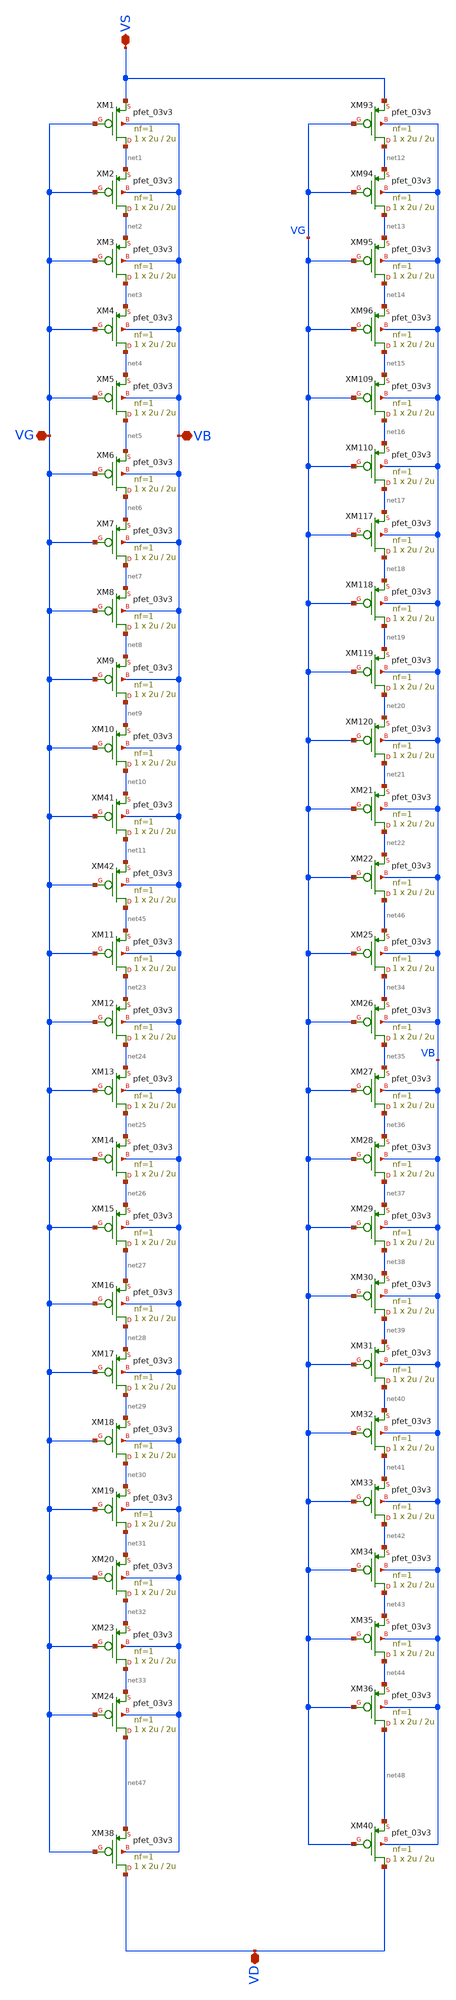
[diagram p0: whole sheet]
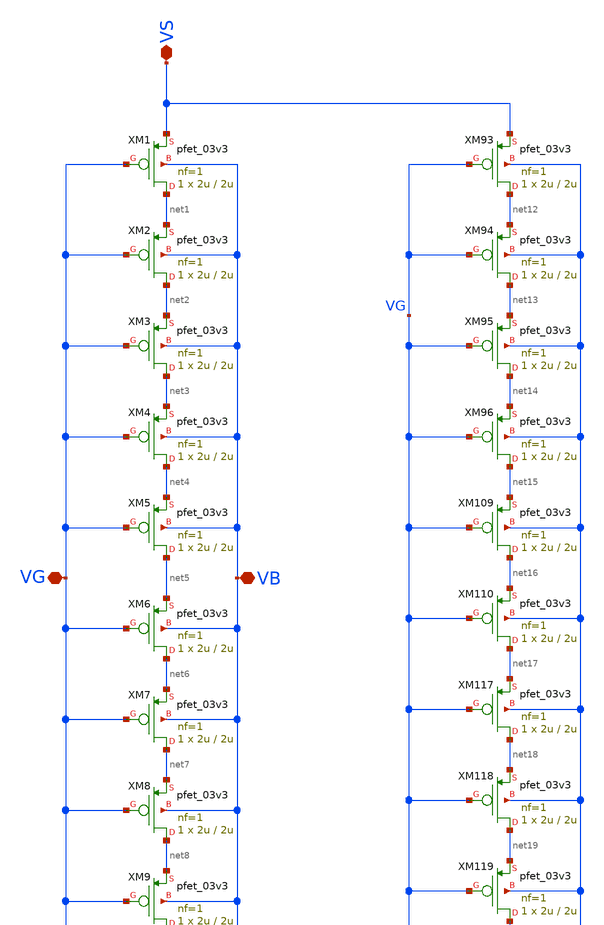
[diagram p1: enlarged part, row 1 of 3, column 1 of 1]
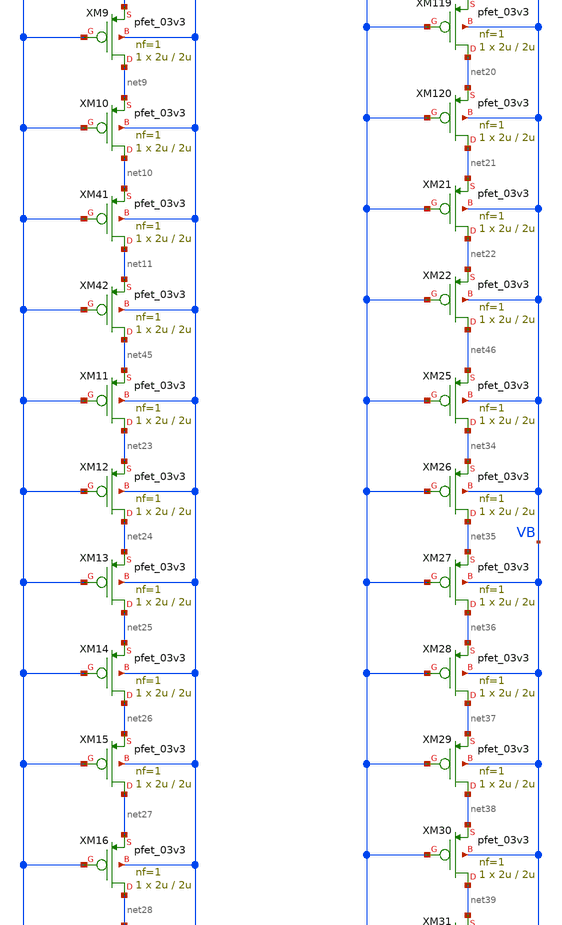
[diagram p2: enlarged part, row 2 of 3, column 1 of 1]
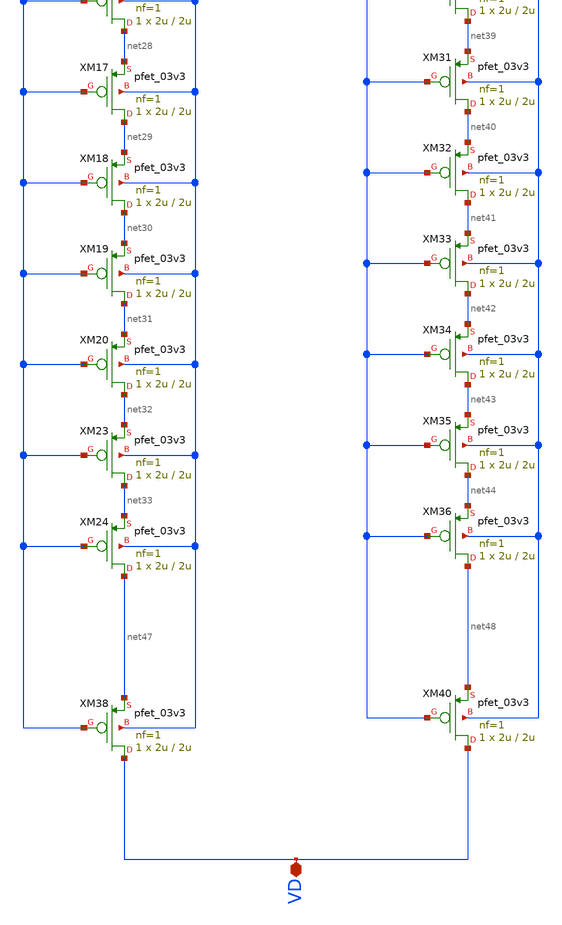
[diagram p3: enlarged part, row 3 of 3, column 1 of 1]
** sch_path: Voltage_Reference/symbols_vr/PMOS_association_1_12.sch
**.subckt PMOS_association_1_12 VD VB VG VS
*.iopin VD
*.iopin VB
*.iopin VG
*.iopin VS
XM1 net1 VG VS VB pfet_03v3 L=2u W=2u nf=1 ad='int((nf+1)/2) * W/nf * 0.18u' as='int((nf+2)/2) * W/nf * 0.18u'
+ pd='2*int((nf+1)/2) * (W/nf + 0.18u)' ps='2*int((nf+2)/2) * (W/nf + 0.18u)' nrd='0.18u / W' nrs='0.18u / W'
+ sa=0 sb=0 sd=0 m=1
XM2 net2 VG net1 VB pfet_03v3 L=2u W=2u nf=1 ad='int((nf+1)/2) * W/nf * 0.18u' as='int((nf+2)/2) * W/nf * 0.18u'
+ pd='2*int((nf+1)/2) * (W/nf + 0.18u)' ps='2*int((nf+2)/2) * (W/nf + 0.18u)' nrd='0.18u / W' nrs='0.18u / W'
+ sa=0 sb=0 sd=0 m=1
XM3 net3 VG net2 VB pfet_03v3 L=2u W=2u nf=1 ad='int((nf+1)/2) * W/nf * 0.18u' as='int((nf+2)/2) * W/nf * 0.18u'
+ pd='2*int((nf+1)/2) * (W/nf + 0.18u)' ps='2*int((nf+2)/2) * (W/nf + 0.18u)' nrd='0.18u / W' nrs='0.18u / W'
+ sa=0 sb=0 sd=0 m=1
XM4 net4 VG net3 VB pfet_03v3 L=2u W=2u nf=1 ad='int((nf+1)/2) * W/nf * 0.18u' as='int((nf+2)/2) * W/nf * 0.18u'
+ pd='2*int((nf+1)/2) * (W/nf + 0.18u)' ps='2*int((nf+2)/2) * (W/nf + 0.18u)' nrd='0.18u / W' nrs='0.18u / W'
+ sa=0 sb=0 sd=0 m=1
XM5 net5 VG net4 VB pfet_03v3 L=2u W=2u nf=1 ad='int((nf+1)/2) * W/nf * 0.18u' as='int((nf+2)/2) * W/nf * 0.18u'
+ pd='2*int((nf+1)/2) * (W/nf + 0.18u)' ps='2*int((nf+2)/2) * (W/nf + 0.18u)' nrd='0.18u / W' nrs='0.18u / W'
+ sa=0 sb=0 sd=0 m=1
XM6 net6 VG net5 VB pfet_03v3 L=2u W=2u nf=1 ad='int((nf+1)/2) * W/nf * 0.18u' as='int((nf+2)/2) * W/nf * 0.18u'
+ pd='2*int((nf+1)/2) * (W/nf + 0.18u)' ps='2*int((nf+2)/2) * (W/nf + 0.18u)' nrd='0.18u / W' nrs='0.18u / W'
+ sa=0 sb=0 sd=0 m=1
XM7 net7 VG net6 VB pfet_03v3 L=2u W=2u nf=1 ad='int((nf+1)/2) * W/nf * 0.18u' as='int((nf+2)/2) * W/nf * 0.18u'
+ pd='2*int((nf+1)/2) * (W/nf + 0.18u)' ps='2*int((nf+2)/2) * (W/nf + 0.18u)' nrd='0.18u / W' nrs='0.18u / W'
+ sa=0 sb=0 sd=0 m=1
XM8 net8 VG net7 VB pfet_03v3 L=2u W=2u nf=1 ad='int((nf+1)/2) * W/nf * 0.18u' as='int((nf+2)/2) * W/nf * 0.18u'
+ pd='2*int((nf+1)/2) * (W/nf + 0.18u)' ps='2*int((nf+2)/2) * (W/nf + 0.18u)' nrd='0.18u / W' nrs='0.18u / W'
+ sa=0 sb=0 sd=0 m=1
XM9 net9 VG net8 VB pfet_03v3 L=2u W=2u nf=1 ad='int((nf+1)/2) * W/nf * 0.18u' as='int((nf+2)/2) * W/nf * 0.18u'
+ pd='2*int((nf+1)/2) * (W/nf + 0.18u)' ps='2*int((nf+2)/2) * (W/nf + 0.18u)' nrd='0.18u / W' nrs='0.18u / W'
+ sa=0 sb=0 sd=0 m=1
XM10 net10 VG net9 VB pfet_03v3 L=2u W=2u nf=1 ad='int((nf+1)/2) * W/nf * 0.18u' as='int((nf+2)/2) * W/nf * 0.18u'
+ pd='2*int((nf+1)/2) * (W/nf + 0.18u)' ps='2*int((nf+2)/2) * (W/nf + 0.18u)' nrd='0.18u / W' nrs='0.18u / W'
+ sa=0 sb=0 sd=0 m=1
XM41 net11 VG net10 VB pfet_03v3 L=2u W=2u nf=1 ad='int((nf+1)/2) * W/nf * 0.18u' as='int((nf+2)/2) * W/nf * 0.18u'
+ pd='2*int((nf+1)/2) * (W/nf + 0.18u)' ps='2*int((nf+2)/2) * (W/nf + 0.18u)' nrd='0.18u / W' nrs='0.18u / W'
+ sa=0 sb=0 sd=0 m=1
XM42 net45 VG net11 VB pfet_03v3 L=2u W=2u nf=1 ad='int((nf+1)/2) * W/nf * 0.18u' as='int((nf+2)/2) * W/nf * 0.18u'
+ pd='2*int((nf+1)/2) * (W/nf + 0.18u)' ps='2*int((nf+2)/2) * (W/nf + 0.18u)' nrd='0.18u / W' nrs='0.18u / W'
+ sa=0 sb=0 sd=0 m=1
XM93 net12 VG VS VB pfet_03v3 L=2u W=2u nf=1 ad='int((nf+1)/2) * W/nf * 0.18u' as='int((nf+2)/2) * W/nf * 0.18u'
+ pd='2*int((nf+1)/2) * (W/nf + 0.18u)' ps='2*int((nf+2)/2) * (W/nf + 0.18u)' nrd='0.18u / W' nrs='0.18u / W'
+ sa=0 sb=0 sd=0 m=1
XM94 net13 VG net12 VB pfet_03v3 L=2u W=2u nf=1 ad='int((nf+1)/2) * W/nf * 0.18u' as='int((nf+2)/2) * W/nf * 0.18u'
+ pd='2*int((nf+1)/2) * (W/nf + 0.18u)' ps='2*int((nf+2)/2) * (W/nf + 0.18u)' nrd='0.18u / W' nrs='0.18u / W'
+ sa=0 sb=0 sd=0 m=1
XM95 net14 VG net13 VB pfet_03v3 L=2u W=2u nf=1 ad='int((nf+1)/2) * W/nf * 0.18u' as='int((nf+2)/2) * W/nf * 0.18u'
+ pd='2*int((nf+1)/2) * (W/nf + 0.18u)' ps='2*int((nf+2)/2) * (W/nf + 0.18u)' nrd='0.18u / W' nrs='0.18u / W'
+ sa=0 sb=0 sd=0 m=1
XM96 net15 VG net14 VB pfet_03v3 L=2u W=2u nf=1 ad='int((nf+1)/2) * W/nf * 0.18u' as='int((nf+2)/2) * W/nf * 0.18u'
+ pd='2*int((nf+1)/2) * (W/nf + 0.18u)' ps='2*int((nf+2)/2) * (W/nf + 0.18u)' nrd='0.18u / W' nrs='0.18u / W'
+ sa=0 sb=0 sd=0 m=1
XM109 net16 VG net15 VB pfet_03v3 L=2u W=2u nf=1 ad='int((nf+1)/2) * W/nf * 0.18u' as='int((nf+2)/2) * W/nf * 0.18u'
+ pd='2*int((nf+1)/2) * (W/nf + 0.18u)' ps='2*int((nf+2)/2) * (W/nf + 0.18u)' nrd='0.18u / W' nrs='0.18u / W'
+ sa=0 sb=0 sd=0 m=1
XM110 net17 VG net16 VB pfet_03v3 L=2u W=2u nf=1 ad='int((nf+1)/2) * W/nf * 0.18u' as='int((nf+2)/2) * W/nf * 0.18u'
+ pd='2*int((nf+1)/2) * (W/nf + 0.18u)' ps='2*int((nf+2)/2) * (W/nf + 0.18u)' nrd='0.18u / W' nrs='0.18u / W'
+ sa=0 sb=0 sd=0 m=1
XM117 net18 VG net17 VB pfet_03v3 L=2u W=2u nf=1 ad='int((nf+1)/2) * W/nf * 0.18u' as='int((nf+2)/2) * W/nf * 0.18u'
+ pd='2*int((nf+1)/2) * (W/nf + 0.18u)' ps='2*int((nf+2)/2) * (W/nf + 0.18u)' nrd='0.18u / W' nrs='0.18u / W'
+ sa=0 sb=0 sd=0 m=1
XM118 net19 VG net18 VB pfet_03v3 L=2u W=2u nf=1 ad='int((nf+1)/2) * W/nf * 0.18u' as='int((nf+2)/2) * W/nf * 0.18u'
+ pd='2*int((nf+1)/2) * (W/nf + 0.18u)' ps='2*int((nf+2)/2) * (W/nf + 0.18u)' nrd='0.18u / W' nrs='0.18u / W'
+ sa=0 sb=0 sd=0 m=1
XM119 net20 VG net19 VB pfet_03v3 L=2u W=2u nf=1 ad='int((nf+1)/2) * W/nf * 0.18u' as='int((nf+2)/2) * W/nf * 0.18u'
+ pd='2*int((nf+1)/2) * (W/nf + 0.18u)' ps='2*int((nf+2)/2) * (W/nf + 0.18u)' nrd='0.18u / W' nrs='0.18u / W'
+ sa=0 sb=0 sd=0 m=1
XM120 net21 VG net20 VB pfet_03v3 L=2u W=2u nf=1 ad='int((nf+1)/2) * W/nf * 0.18u' as='int((nf+2)/2) * W/nf * 0.18u'
+ pd='2*int((nf+1)/2) * (W/nf + 0.18u)' ps='2*int((nf+2)/2) * (W/nf + 0.18u)' nrd='0.18u / W' nrs='0.18u / W'
+ sa=0 sb=0 sd=0 m=1
XM21 net22 VG net21 VB pfet_03v3 L=2u W=2u nf=1 ad='int((nf+1)/2) * W/nf * 0.18u' as='int((nf+2)/2) * W/nf * 0.18u'
+ pd='2*int((nf+1)/2) * (W/nf + 0.18u)' ps='2*int((nf+2)/2) * (W/nf + 0.18u)' nrd='0.18u / W' nrs='0.18u / W'
+ sa=0 sb=0 sd=0 m=1
XM22 net46 VG net22 VB pfet_03v3 L=2u W=2u nf=1 ad='int((nf+1)/2) * W/nf * 0.18u' as='int((nf+2)/2) * W/nf * 0.18u'
+ pd='2*int((nf+1)/2) * (W/nf + 0.18u)' ps='2*int((nf+2)/2) * (W/nf + 0.18u)' nrd='0.18u / W' nrs='0.18u / W'
+ sa=0 sb=0 sd=0 m=1
XM11 net23 VG net45 VB pfet_03v3 L=2u W=2u nf=1 ad='int((nf+1)/2) * W/nf * 0.18u' as='int((nf+2)/2) * W/nf * 0.18u'
+ pd='2*int((nf+1)/2) * (W/nf + 0.18u)' ps='2*int((nf+2)/2) * (W/nf + 0.18u)' nrd='0.18u / W' nrs='0.18u / W'
+ sa=0 sb=0 sd=0 m=1
XM12 net24 VG net23 VB pfet_03v3 L=2u W=2u nf=1 ad='int((nf+1)/2) * W/nf * 0.18u' as='int((nf+2)/2) * W/nf * 0.18u'
+ pd='2*int((nf+1)/2) * (W/nf + 0.18u)' ps='2*int((nf+2)/2) * (W/nf + 0.18u)' nrd='0.18u / W' nrs='0.18u / W'
+ sa=0 sb=0 sd=0 m=1
XM13 net25 VG net24 VB pfet_03v3 L=2u W=2u nf=1 ad='int((nf+1)/2) * W/nf * 0.18u' as='int((nf+2)/2) * W/nf * 0.18u'
+ pd='2*int((nf+1)/2) * (W/nf + 0.18u)' ps='2*int((nf+2)/2) * (W/nf + 0.18u)' nrd='0.18u / W' nrs='0.18u / W'
+ sa=0 sb=0 sd=0 m=1
XM14 net26 VG net25 VB pfet_03v3 L=2u W=2u nf=1 ad='int((nf+1)/2) * W/nf * 0.18u' as='int((nf+2)/2) * W/nf * 0.18u'
+ pd='2*int((nf+1)/2) * (W/nf + 0.18u)' ps='2*int((nf+2)/2) * (W/nf + 0.18u)' nrd='0.18u / W' nrs='0.18u / W'
+ sa=0 sb=0 sd=0 m=1
XM15 net27 VG net26 VB pfet_03v3 L=2u W=2u nf=1 ad='int((nf+1)/2) * W/nf * 0.18u' as='int((nf+2)/2) * W/nf * 0.18u'
+ pd='2*int((nf+1)/2) * (W/nf + 0.18u)' ps='2*int((nf+2)/2) * (W/nf + 0.18u)' nrd='0.18u / W' nrs='0.18u / W'
+ sa=0 sb=0 sd=0 m=1
XM16 net28 VG net27 VB pfet_03v3 L=2u W=2u nf=1 ad='int((nf+1)/2) * W/nf * 0.18u' as='int((nf+2)/2) * W/nf * 0.18u'
+ pd='2*int((nf+1)/2) * (W/nf + 0.18u)' ps='2*int((nf+2)/2) * (W/nf + 0.18u)' nrd='0.18u / W' nrs='0.18u / W'
+ sa=0 sb=0 sd=0 m=1
XM17 net29 VG net28 VB pfet_03v3 L=2u W=2u nf=1 ad='int((nf+1)/2) * W/nf * 0.18u' as='int((nf+2)/2) * W/nf * 0.18u'
+ pd='2*int((nf+1)/2) * (W/nf + 0.18u)' ps='2*int((nf+2)/2) * (W/nf + 0.18u)' nrd='0.18u / W' nrs='0.18u / W'
+ sa=0 sb=0 sd=0 m=1
XM18 net30 VG net29 VB pfet_03v3 L=2u W=2u nf=1 ad='int((nf+1)/2) * W/nf * 0.18u' as='int((nf+2)/2) * W/nf * 0.18u'
+ pd='2*int((nf+1)/2) * (W/nf + 0.18u)' ps='2*int((nf+2)/2) * (W/nf + 0.18u)' nrd='0.18u / W' nrs='0.18u / W'
+ sa=0 sb=0 sd=0 m=1
XM19 net31 VG net30 VB pfet_03v3 L=2u W=2u nf=1 ad='int((nf+1)/2) * W/nf * 0.18u' as='int((nf+2)/2) * W/nf * 0.18u'
+ pd='2*int((nf+1)/2) * (W/nf + 0.18u)' ps='2*int((nf+2)/2) * (W/nf + 0.18u)' nrd='0.18u / W' nrs='0.18u / W'
+ sa=0 sb=0 sd=0 m=1
XM20 net32 VG net31 VB pfet_03v3 L=2u W=2u nf=1 ad='int((nf+1)/2) * W/nf * 0.18u' as='int((nf+2)/2) * W/nf * 0.18u'
+ pd='2*int((nf+1)/2) * (W/nf + 0.18u)' ps='2*int((nf+2)/2) * (W/nf + 0.18u)' nrd='0.18u / W' nrs='0.18u / W'
+ sa=0 sb=0 sd=0 m=1
XM23 net33 VG net32 VB pfet_03v3 L=2u W=2u nf=1 ad='int((nf+1)/2) * W/nf * 0.18u' as='int((nf+2)/2) * W/nf * 0.18u'
+ pd='2*int((nf+1)/2) * (W/nf + 0.18u)' ps='2*int((nf+2)/2) * (W/nf + 0.18u)' nrd='0.18u / W' nrs='0.18u / W'
+ sa=0 sb=0 sd=0 m=1
XM24 net47 VG net33 VB pfet_03v3 L=2u W=2u nf=1 ad='int((nf+1)/2) * W/nf * 0.18u' as='int((nf+2)/2) * W/nf * 0.18u'
+ pd='2*int((nf+1)/2) * (W/nf + 0.18u)' ps='2*int((nf+2)/2) * (W/nf + 0.18u)' nrd='0.18u / W' nrs='0.18u / W'
+ sa=0 sb=0 sd=0 m=1
XM25 net34 VG net46 VB pfet_03v3 L=2u W=2u nf=1 ad='int((nf+1)/2) * W/nf * 0.18u' as='int((nf+2)/2) * W/nf * 0.18u'
+ pd='2*int((nf+1)/2) * (W/nf + 0.18u)' ps='2*int((nf+2)/2) * (W/nf + 0.18u)' nrd='0.18u / W' nrs='0.18u / W'
+ sa=0 sb=0 sd=0 m=1
XM26 net35 VG net34 VB pfet_03v3 L=2u W=2u nf=1 ad='int((nf+1)/2) * W/nf * 0.18u' as='int((nf+2)/2) * W/nf * 0.18u'
+ pd='2*int((nf+1)/2) * (W/nf + 0.18u)' ps='2*int((nf+2)/2) * (W/nf + 0.18u)' nrd='0.18u / W' nrs='0.18u / W'
+ sa=0 sb=0 sd=0 m=1
XM27 net36 VG net35 VB pfet_03v3 L=2u W=2u nf=1 ad='int((nf+1)/2) * W/nf * 0.18u' as='int((nf+2)/2) * W/nf * 0.18u'
+ pd='2*int((nf+1)/2) * (W/nf + 0.18u)' ps='2*int((nf+2)/2) * (W/nf + 0.18u)' nrd='0.18u / W' nrs='0.18u / W'
+ sa=0 sb=0 sd=0 m=1
XM28 net37 VG net36 VB pfet_03v3 L=2u W=2u nf=1 ad='int((nf+1)/2) * W/nf * 0.18u' as='int((nf+2)/2) * W/nf * 0.18u'
+ pd='2*int((nf+1)/2) * (W/nf + 0.18u)' ps='2*int((nf+2)/2) * (W/nf + 0.18u)' nrd='0.18u / W' nrs='0.18u / W'
+ sa=0 sb=0 sd=0 m=1
XM29 net38 VG net37 VB pfet_03v3 L=2u W=2u nf=1 ad='int((nf+1)/2) * W/nf * 0.18u' as='int((nf+2)/2) * W/nf * 0.18u'
+ pd='2*int((nf+1)/2) * (W/nf + 0.18u)' ps='2*int((nf+2)/2) * (W/nf + 0.18u)' nrd='0.18u / W' nrs='0.18u / W'
+ sa=0 sb=0 sd=0 m=1
XM30 net39 VG net38 VB pfet_03v3 L=2u W=2u nf=1 ad='int((nf+1)/2) * W/nf * 0.18u' as='int((nf+2)/2) * W/nf * 0.18u'
+ pd='2*int((nf+1)/2) * (W/nf + 0.18u)' ps='2*int((nf+2)/2) * (W/nf + 0.18u)' nrd='0.18u / W' nrs='0.18u / W'
+ sa=0 sb=0 sd=0 m=1
XM31 net40 VG net39 VB pfet_03v3 L=2u W=2u nf=1 ad='int((nf+1)/2) * W/nf * 0.18u' as='int((nf+2)/2) * W/nf * 0.18u'
+ pd='2*int((nf+1)/2) * (W/nf + 0.18u)' ps='2*int((nf+2)/2) * (W/nf + 0.18u)' nrd='0.18u / W' nrs='0.18u / W'
+ sa=0 sb=0 sd=0 m=1
XM32 net41 VG net40 VB pfet_03v3 L=2u W=2u nf=1 ad='int((nf+1)/2) * W/nf * 0.18u' as='int((nf+2)/2) * W/nf * 0.18u'
+ pd='2*int((nf+1)/2) * (W/nf + 0.18u)' ps='2*int((nf+2)/2) * (W/nf + 0.18u)' nrd='0.18u / W' nrs='0.18u / W'
+ sa=0 sb=0 sd=0 m=1
XM33 net42 VG net41 VB pfet_03v3 L=2u W=2u nf=1 ad='int((nf+1)/2) * W/nf * 0.18u' as='int((nf+2)/2) * W/nf * 0.18u'
+ pd='2*int((nf+1)/2) * (W/nf + 0.18u)' ps='2*int((nf+2)/2) * (W/nf + 0.18u)' nrd='0.18u / W' nrs='0.18u / W'
+ sa=0 sb=0 sd=0 m=1
XM34 net43 VG net42 VB pfet_03v3 L=2u W=2u nf=1 ad='int((nf+1)/2) * W/nf * 0.18u' as='int((nf+2)/2) * W/nf * 0.18u'
+ pd='2*int((nf+1)/2) * (W/nf + 0.18u)' ps='2*int((nf+2)/2) * (W/nf + 0.18u)' nrd='0.18u / W' nrs='0.18u / W'
+ sa=0 sb=0 sd=0 m=1
XM35 net44 VG net43 VB pfet_03v3 L=2u W=2u nf=1 ad='int((nf+1)/2) * W/nf * 0.18u' as='int((nf+2)/2) * W/nf * 0.18u'
+ pd='2*int((nf+1)/2) * (W/nf + 0.18u)' ps='2*int((nf+2)/2) * (W/nf + 0.18u)' nrd='0.18u / W' nrs='0.18u / W'
+ sa=0 sb=0 sd=0 m=1
XM36 net48 VG net44 VB pfet_03v3 L=2u W=2u nf=1 ad='int((nf+1)/2) * W/nf * 0.18u' as='int((nf+2)/2) * W/nf * 0.18u'
+ pd='2*int((nf+1)/2) * (W/nf + 0.18u)' ps='2*int((nf+2)/2) * (W/nf + 0.18u)' nrd='0.18u / W' nrs='0.18u / W'
+ sa=0 sb=0 sd=0 m=1
XM38 VD VG net47 VB pfet_03v3 L=2u W=2u nf=1 ad='int((nf+1)/2) * W/nf * 0.18u' as='int((nf+2)/2) * W/nf * 0.18u'
+ pd='2*int((nf+1)/2) * (W/nf + 0.18u)' ps='2*int((nf+2)/2) * (W/nf + 0.18u)' nrd='0.18u / W' nrs='0.18u / W'
+ sa=0 sb=0 sd=0 m=1
XM40 VD VG net48 VB pfet_03v3 L=2u W=2u nf=1 ad='int((nf+1)/2) * W/nf * 0.18u' as='int((nf+2)/2) * W/nf * 0.18u'
+ pd='2*int((nf+1)/2) * (W/nf + 0.18u)' ps='2*int((nf+2)/2) * (W/nf + 0.18u)' nrd='0.18u / W' nrs='0.18u / W'
+ sa=0 sb=0 sd=0 m=1
**.ends
.end
